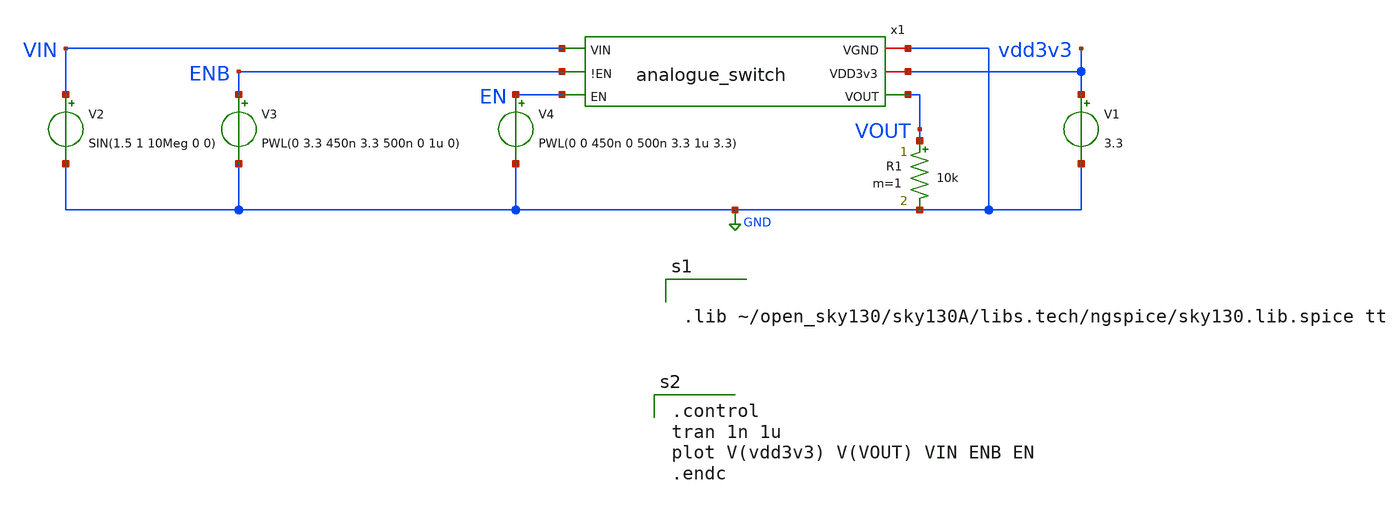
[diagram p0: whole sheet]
** sch_path: xschem/analogue_switch_tb.sch
**.subckt analogue_switch_tb
x1 VIN GND vdd3v3 ENB EN VOUT analogue_switch
V1 vdd3v3 GND 3.3
V2 VIN GND SIN(1.5 1 10Meg 0 0)
V3 ENB GND PWL(0 3.3 450n 3.3 500n 0 1u 0)
V4 EN GND PWL(0 0 450n 0 500n 3.3 1u 3.3)
R1 VOUT GND 10k m=1
**** begin user architecture code


.lib ~/open_sky130/sky130A/libs.tech/ngspice/sky130.lib.spice tt


.control
tran 1n 1u
plot V(vdd3v3) V(VOUT) VIN ENB EN
.endc

**** end user architecture code
**.ends

* expanding   symbol:  analogue_switch.sym # of pins=6
** sym_path: xschem/analogue_switch.sym
** sch_path: xschem/analogue_switch.sch
.subckt analogue_switch VIN VGND VDD3v3 !EN EN VOUT
*.iopin VGND
*.iopin VDD3v3
*.ipin EN
*.ipin VIN
*.ipin !EN
*.opin VOUT
XM2 VOUT !EN VIN VDD3v3 sky130_fd_pr__pfet_g5v0d10v5 L=0.5 W=1 nf=1 ad='int((nf+1)/2) * W/nf * 0.29'
+ as='int((nf+2)/2) * W/nf * 0.29' pd='2*int((nf+1)/2) * (W/nf + 0.29)' ps='2*int((nf+2)/2) * (W/nf + 0.29)'
+ nrd='0.29 / W' nrs='0.29 / W' sa=0 sb=0 sd=0 mult=1 m=1
XM1 VIN EN VOUT VGND sky130_fd_pr__nfet_03v3_nvt L=0.5 W=1 nf=1 ad='int((nf+1)/2) * W/nf * 0.29' as='int((nf+2)/2) * W/nf * 0.29'
+ pd='2*int((nf+1)/2) * (W/nf + 0.29)' ps='2*int((nf+2)/2) * (W/nf + 0.29)' nrd='0.29 / W' nrs='0.29 / W'
+ sa=0 sb=0 sd=0 mult=1 m=1
.ends

.GLOBAL GND
.end
